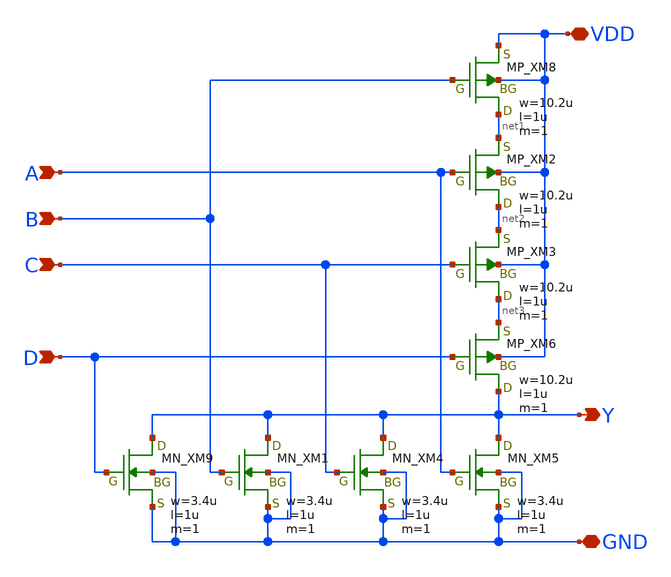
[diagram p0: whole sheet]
** sch_path: openIP62_rev1.0/IP62/Technology/tech/symbols/Xschem/IP62_5_stdcell/NOR4.sch
**.subckt NOR4 A B Y VDD GND C D
*.ipin A
*.ipin B
*.opin Y
*.iopin VDD
*.iopin GND
*.ipin C
*.ipin D
XM8 net1 B VDD VDD PMOS w=10.2u l=1u as=0 ad=0 ps=0 pd=0 nrd=0 nrs=0 m=1
XM2 net2 A net1 VDD PMOS w=10.2u l=1u as=0 ad=0 ps=0 pd=0 nrd=0 nrs=0 m=1
XM3 net3 C net2 VDD PMOS w=10.2u l=1u as=0 ad=0 ps=0 pd=0 nrd=0 nrs=0 m=1
XM6 Y D net3 VDD PMOS w=10.2u l=1u as=0 ad=0 ps=0 pd=0 nrd=0 nrs=0 m=1
XM9 Y D GND GND NMOS w=3.4u l=1u as=0 ad=0 ps=0 pd=0 nrd=0 nrs=0 m=1
XM1 Y B GND GND NMOS w=3.4u l=1u as=0 ad=0 ps=0 pd=0 nrd=0 nrs=0 m=1
XM4 Y C GND GND NMOS w=3.4u l=1u as=0 ad=0 ps=0 pd=0 nrd=0 nrs=0 m=1
XM5 Y A GND GND NMOS w=3.4u l=1u as=0 ad=0 ps=0 pd=0 nrd=0 nrs=0 m=1
**.ends
.end
